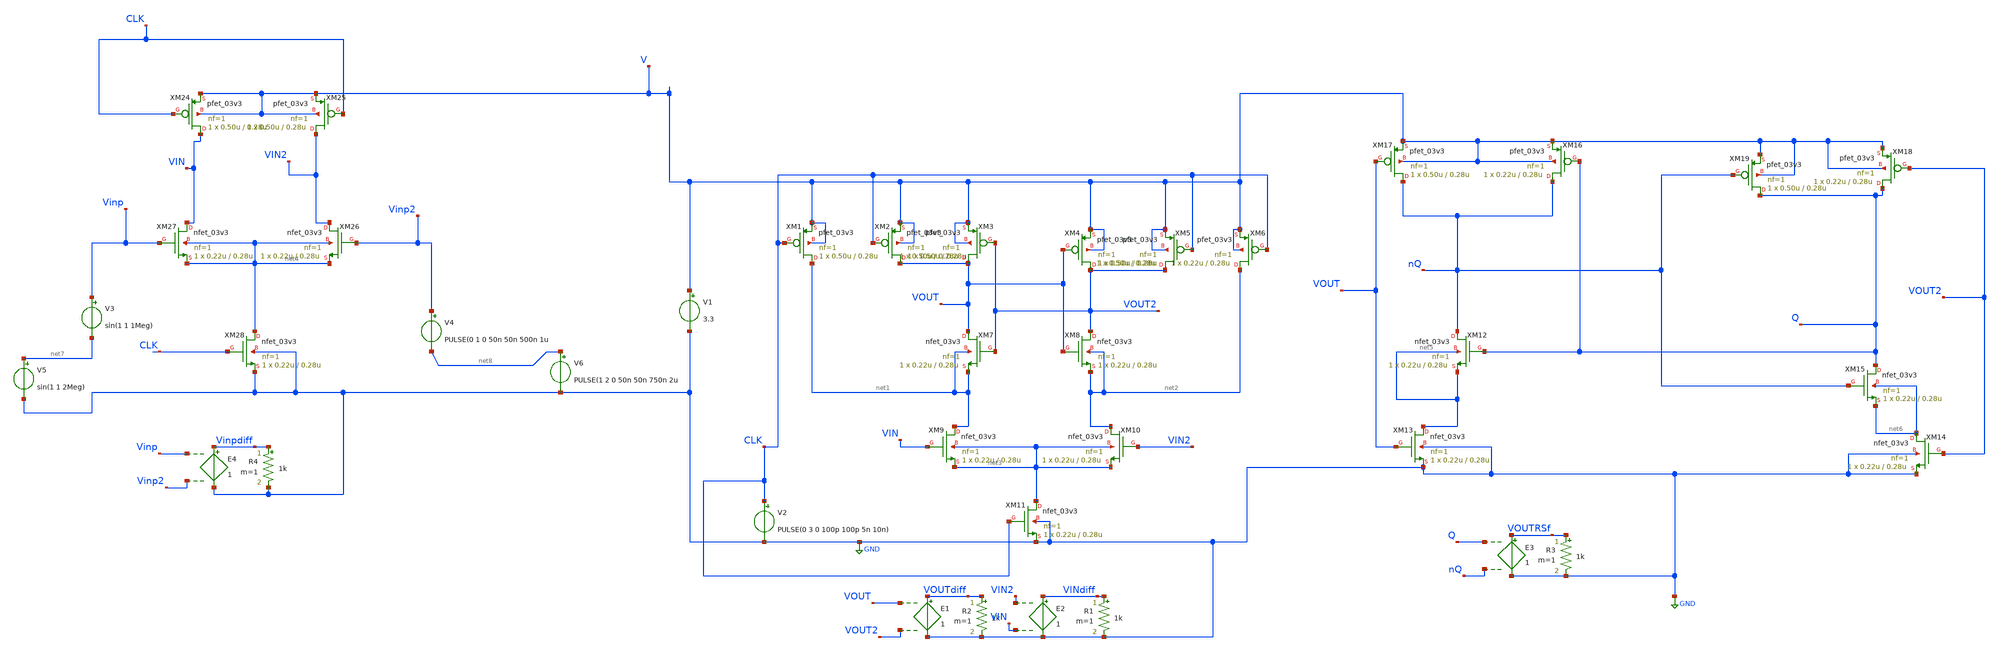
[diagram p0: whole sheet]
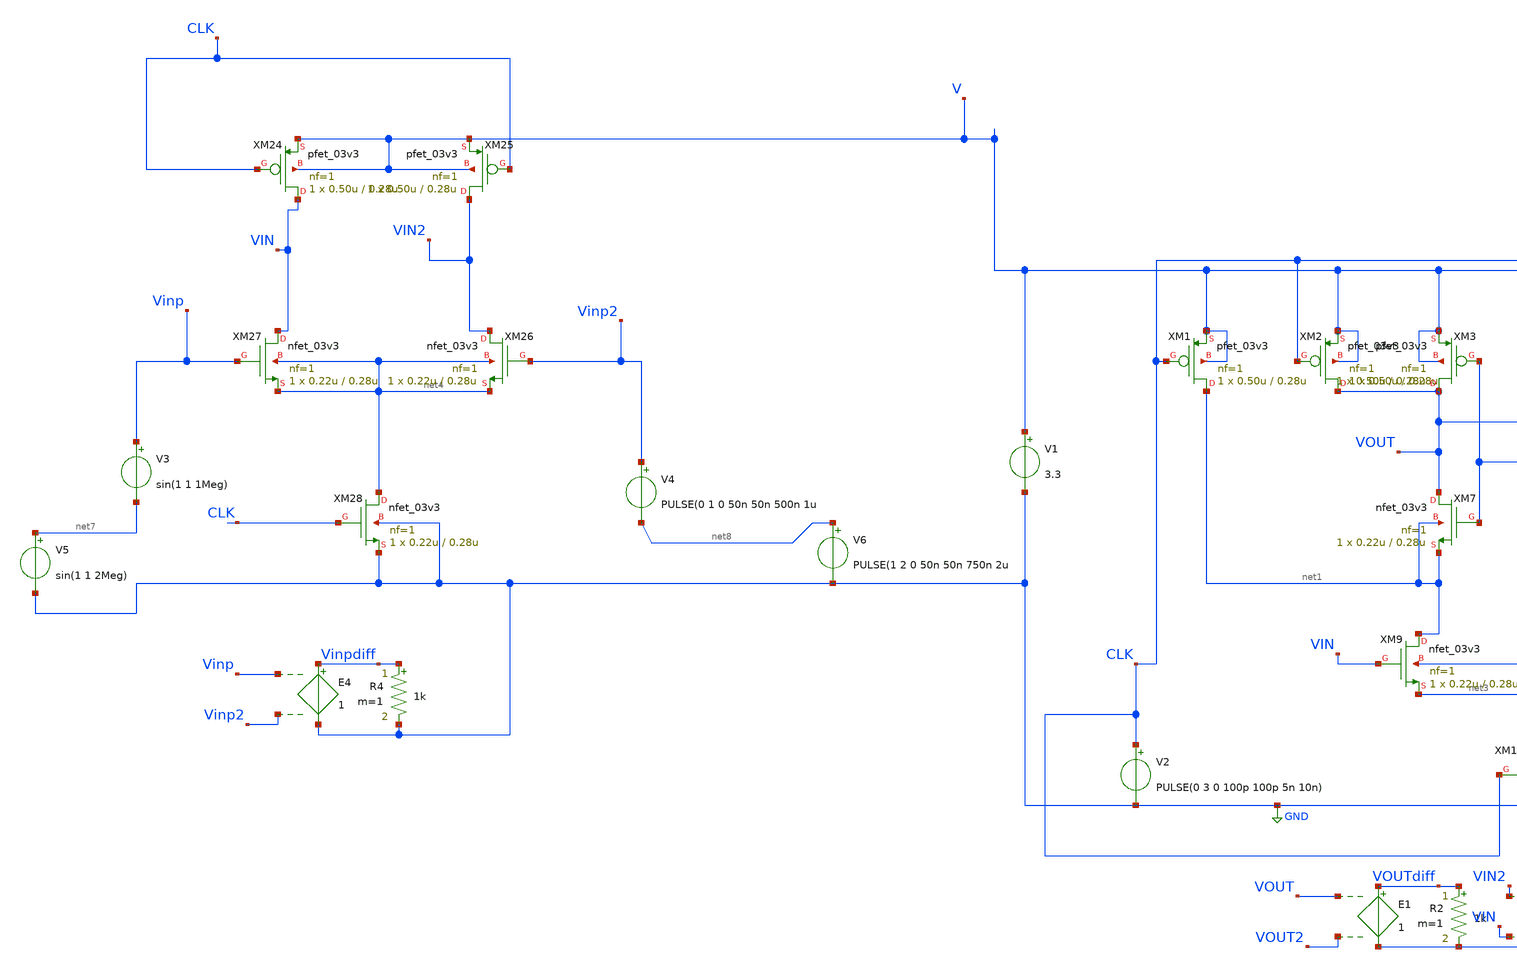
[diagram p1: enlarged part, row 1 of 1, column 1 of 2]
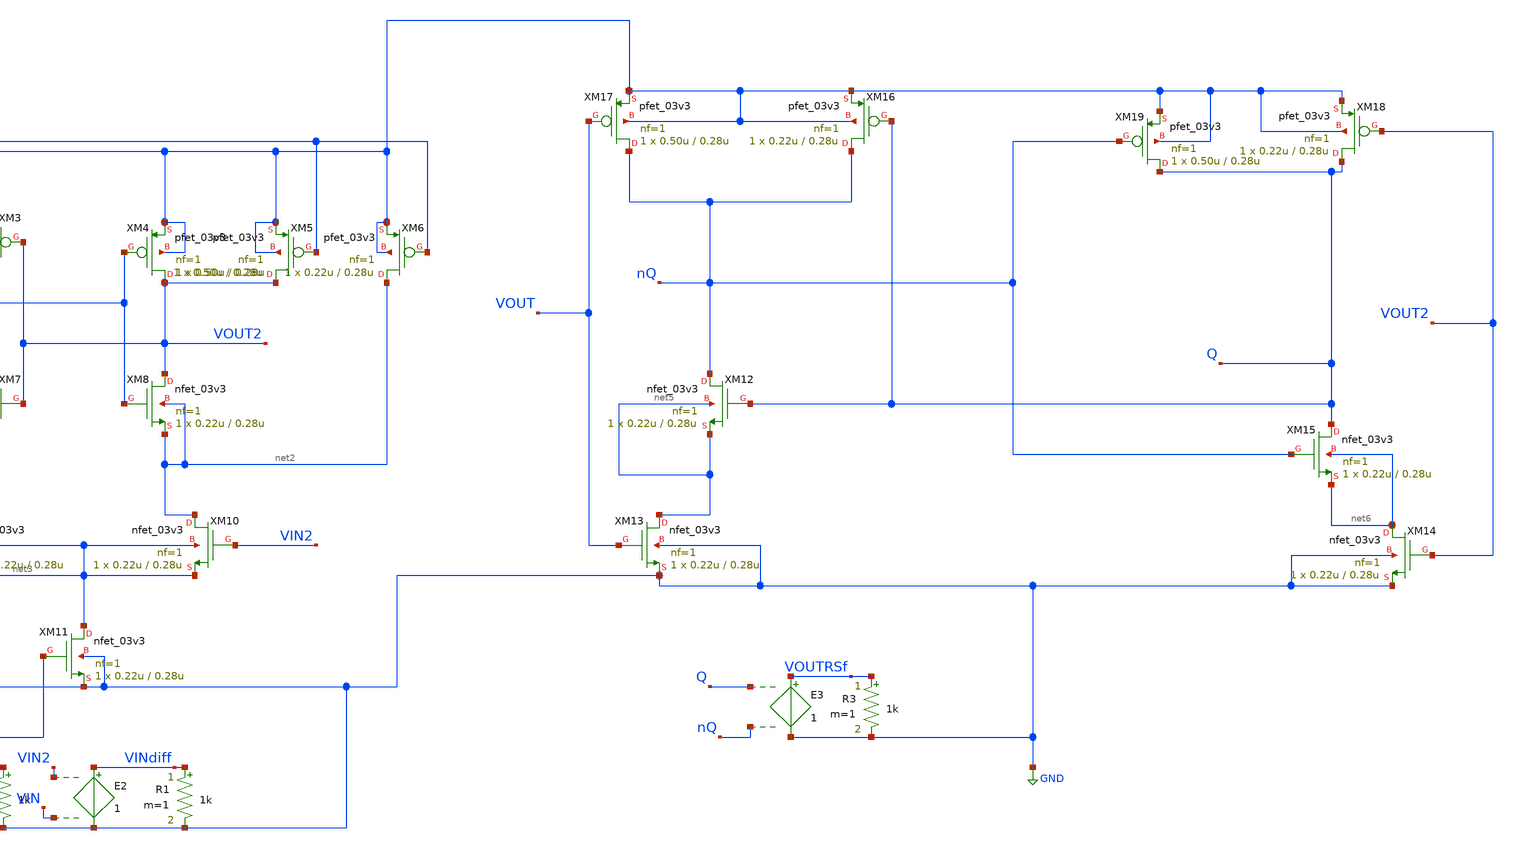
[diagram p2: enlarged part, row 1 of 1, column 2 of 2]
** sch_path: old/StrongArm2.sch
**.subckt StrongArm2
XM1 net1 CLK V V pfet_03v3 L=0.28u W=0.50u nf=1 ad='int((nf+1)/2) * W/nf * 0.18u' as='int((nf+2)/2) * W/nf * 0.18u'
+ pd='2*int((nf+1)/2) * (W/nf + 0.18u)' ps='2*int((nf+2)/2) * (W/nf + 0.18u)' nrd='0.18u / W' nrs='0.18u / W'
+ sa=0 sb=0 sd=0 m=1
XM2 VOUT CLK V V pfet_03v3 L=0.28u W=0.50u nf=1 ad='int((nf+1)/2) * W/nf * 0.18u' as='int((nf+2)/2) * W/nf * 0.18u'
+ pd='2*int((nf+1)/2) * (W/nf + 0.18u)' ps='2*int((nf+2)/2) * (W/nf + 0.18u)' nrd='0.18u / W' nrs='0.18u / W'
+ sa=0 sb=0 sd=0 m=1
XM3 VOUT VOUT2 V V pfet_03v3 L=0.28u W=0.50u nf=1 ad='int((nf+1)/2) * W/nf * 0.18u' as='int((nf+2)/2) * W/nf * 0.18u'
+ pd='2*int((nf+1)/2) * (W/nf + 0.18u)' ps='2*int((nf+2)/2) * (W/nf + 0.18u)' nrd='0.18u / W' nrs='0.18u / W'
+ sa=0 sb=0 sd=0 m=1
XM4 VOUT2 VOUT V V pfet_03v3 L=0.28u W=0.50u nf=1 ad='int((nf+1)/2) * W/nf * 0.18u' as='int((nf+2)/2) * W/nf * 0.18u'
+ pd='2*int((nf+1)/2) * (W/nf + 0.18u)' ps='2*int((nf+2)/2) * (W/nf + 0.18u)' nrd='0.18u / W' nrs='0.18u / W'
+ sa=0 sb=0 sd=0 m=1
XM5 VOUT2 CLK V V pfet_03v3 L=0.28u W=0.50u nf=1 ad='int((nf+1)/2) * W/nf * 0.18u' as='int((nf+2)/2) * W/nf * 0.18u'
+ pd='2*int((nf+1)/2) * (W/nf + 0.18u)' ps='2*int((nf+2)/2) * (W/nf + 0.18u)' nrd='0.18u / W' nrs='0.18u / W'
+ sa=0 sb=0 sd=0 m=1
XM6 net2 CLK V V pfet_03v3 L=0.28u W=0.22u nf=1 ad='int((nf+1)/2) * W/nf * 0.18u' as='int((nf+2)/2) * W/nf * 0.18u'
+ pd='2*int((nf+1)/2) * (W/nf + 0.18u)' ps='2*int((nf+2)/2) * (W/nf + 0.18u)' nrd='0.18u / W' nrs='0.18u / W'
+ sa=0 sb=0 sd=0 m=1
XM7 VOUT VOUT2 net1 net1 nfet_03v3 L=0.28u W=0.22u nf=1 ad='int((nf+1)/2) * W/nf * 0.18u' as='int((nf+2)/2) * W/nf * 0.18u'
+ pd='2*int((nf+1)/2) * (W/nf + 0.18u)' ps='2*int((nf+2)/2) * (W/nf + 0.18u)' nrd='0.18u / W' nrs='0.18u / W'
+ sa=0 sb=0 sd=0 m=1
XM8 VOUT2 VOUT net2 net2 nfet_03v3 L=0.28u W=0.22u nf=1 ad='int((nf+1)/2) * W/nf * 0.18u' as='int((nf+2)/2) * W/nf * 0.18u'
+ pd='2*int((nf+1)/2) * (W/nf + 0.18u)' ps='2*int((nf+2)/2) * (W/nf + 0.18u)' nrd='0.18u / W' nrs='0.18u / W'
+ sa=0 sb=0 sd=0 m=1
XM9 net1 VIN net3 net3 nfet_03v3 L=0.28u W=0.22u nf=1 ad='int((nf+1)/2) * W/nf * 0.18u' as='int((nf+2)/2) * W/nf * 0.18u'
+ pd='2*int((nf+1)/2) * (W/nf + 0.18u)' ps='2*int((nf+2)/2) * (W/nf + 0.18u)' nrd='0.18u / W' nrs='0.18u / W'
+ sa=0 sb=0 sd=0 m=1
XM10 net2 VIN2 net3 net3 nfet_03v3 L=0.28u W=0.22u nf=1 ad='int((nf+1)/2) * W/nf * 0.18u' as='int((nf+2)/2) * W/nf * 0.18u'
+ pd='2*int((nf+1)/2) * (W/nf + 0.18u)' ps='2*int((nf+2)/2) * (W/nf + 0.18u)' nrd='0.18u / W' nrs='0.18u / W'
+ sa=0 sb=0 sd=0 m=1
XM11 net3 CLK GND GND nfet_03v3 L=0.28u W=0.22u nf=1 ad='int((nf+1)/2) * W/nf * 0.18u' as='int((nf+2)/2) * W/nf * 0.18u'
+ pd='2*int((nf+1)/2) * (W/nf + 0.18u)' ps='2*int((nf+2)/2) * (W/nf + 0.18u)' nrd='0.18u / W' nrs='0.18u / W'
+ sa=0 sb=0 sd=0 m=1
V1 V GND 3.3
V2 CLK GND PULSE(0 3 0 100p 100p 5n 10n)
R2 VOUTdiff GND 1k m=1
E1 VOUTdiff GND VOUT VOUT2 1
R1 VINdiff GND 1k m=1
E2 VINdiff GND VIN2 VIN 1
XM12 nQ Q net5 net5 nfet_03v3 L=0.28u W=0.22u nf=1 ad='int((nf+1)/2) * W/nf * 0.18u' as='int((nf+2)/2) * W/nf * 0.18u'
+ pd='2*int((nf+1)/2) * (W/nf + 0.18u)' ps='2*int((nf+2)/2) * (W/nf + 0.18u)' nrd='0.18u / W' nrs='0.18u / W'
+ sa=0 sb=0 sd=0 m=1
XM13 net5 VOUT GND GND nfet_03v3 L=0.28u W=0.22u nf=1 ad='int((nf+1)/2) * W/nf * 0.18u' as='int((nf+2)/2) * W/nf * 0.18u'
+ pd='2*int((nf+1)/2) * (W/nf + 0.18u)' ps='2*int((nf+2)/2) * (W/nf + 0.18u)' nrd='0.18u / W' nrs='0.18u / W'
+ sa=0 sb=0 sd=0 m=1
XM14 net6 VOUT2 GND GND nfet_03v3 L=0.28u W=0.22u nf=1 ad='int((nf+1)/2) * W/nf * 0.18u' as='int((nf+2)/2) * W/nf * 0.18u'
+ pd='2*int((nf+1)/2) * (W/nf + 0.18u)' ps='2*int((nf+2)/2) * (W/nf + 0.18u)' nrd='0.18u / W' nrs='0.18u / W'
+ sa=0 sb=0 sd=0 m=1
XM15 Q nQ net6 net6 nfet_03v3 L=0.28u W=0.22u nf=1 ad='int((nf+1)/2) * W/nf * 0.18u' as='int((nf+2)/2) * W/nf * 0.18u'
+ pd='2*int((nf+1)/2) * (W/nf + 0.18u)' ps='2*int((nf+2)/2) * (W/nf + 0.18u)' nrd='0.18u / W' nrs='0.18u / W'
+ sa=0 sb=0 sd=0 m=1
XM16 nQ Q V V pfet_03v3 L=0.28u W=0.22u nf=1 ad='int((nf+1)/2) * W/nf * 0.18u' as='int((nf+2)/2) * W/nf * 0.18u'
+ pd='2*int((nf+1)/2) * (W/nf + 0.18u)' ps='2*int((nf+2)/2) * (W/nf + 0.18u)' nrd='0.18u / W' nrs='0.18u / W'
+ sa=0 sb=0 sd=0 m=1
XM17 nQ VOUT V V pfet_03v3 L=0.28u W=0.50u nf=1 ad='int((nf+1)/2) * W/nf * 0.18u' as='int((nf+2)/2) * W/nf * 0.18u'
+ pd='2*int((nf+1)/2) * (W/nf + 0.18u)' ps='2*int((nf+2)/2) * (W/nf + 0.18u)' nrd='0.18u / W' nrs='0.18u / W'
+ sa=0 sb=0 sd=0 m=1
XM18 Q VOUT2 V V pfet_03v3 L=0.28u W=0.22u nf=1 ad='int((nf+1)/2) * W/nf * 0.18u' as='int((nf+2)/2) * W/nf * 0.18u'
+ pd='2*int((nf+1)/2) * (W/nf + 0.18u)' ps='2*int((nf+2)/2) * (W/nf + 0.18u)' nrd='0.18u / W' nrs='0.18u / W'
+ sa=0 sb=0 sd=0 m=1
XM19 Q nQ V V pfet_03v3 L=0.28u W=0.50u nf=1 ad='int((nf+1)/2) * W/nf * 0.18u' as='int((nf+2)/2) * W/nf * 0.18u'
+ pd='2*int((nf+1)/2) * (W/nf + 0.18u)' ps='2*int((nf+2)/2) * (W/nf + 0.18u)' nrd='0.18u / W' nrs='0.18u / W'
+ sa=0 sb=0 sd=0 m=1
R3 VOUTRSf GND 1k m=1
E3 VOUTRSf GND Q nQ 1
XM26 VIN2 Vinp2 net4 net4 nfet_03v3 L=0.28u W=0.22u nf=1 ad='int((nf+1)/2) * W/nf * 0.18u' as='int((nf+2)/2) * W/nf * 0.18u'
+ pd='2*int((nf+1)/2) * (W/nf + 0.18u)' ps='2*int((nf+2)/2) * (W/nf + 0.18u)' nrd='0.18u / W' nrs='0.18u / W'
+ sa=0 sb=0 sd=0 m=1
XM27 VIN Vinp net4 net4 nfet_03v3 L=0.28u W=0.22u nf=1 ad='int((nf+1)/2) * W/nf * 0.18u' as='int((nf+2)/2) * W/nf * 0.18u'
+ pd='2*int((nf+1)/2) * (W/nf + 0.18u)' ps='2*int((nf+2)/2) * (W/nf + 0.18u)' nrd='0.18u / W' nrs='0.18u / W'
+ sa=0 sb=0 sd=0 m=1
V3 Vinp net7 sin(1 1 1Meg)
V4 Vinp2 net8 PULSE(0 1 0 50n 50n 500n 1u
R4 Vinpdiff GND 1k m=1
E4 Vinpdiff GND Vinp Vinp2 1
XM28 net4 CLK GND GND nfet_03v3 L=0.28u W=0.22u nf=1 ad='int((nf+1)/2) * W/nf * 0.18u' as='int((nf+2)/2) * W/nf * 0.18u'
+ pd='2*int((nf+1)/2) * (W/nf + 0.18u)' ps='2*int((nf+2)/2) * (W/nf + 0.18u)' nrd='0.18u / W' nrs='0.18u / W'
+ sa=0 sb=0 sd=0 m=1
XM24 VIN CLK V V pfet_03v3 L=0.28u W=0.50u nf=1 ad='int((nf+1)/2) * W/nf * 0.18u' as='int((nf+2)/2) * W/nf * 0.18u'
+ pd='2*int((nf+1)/2) * (W/nf + 0.18u)' ps='2*int((nf+2)/2) * (W/nf + 0.18u)' nrd='0.18u / W' nrs='0.18u / W'
+ sa=0 sb=0 sd=0 m=1
XM25 VIN2 CLK V V pfet_03v3 L=0.28u W=0.50u nf=1 ad='int((nf+1)/2) * W/nf * 0.18u' as='int((nf+2)/2) * W/nf * 0.18u'
+ pd='2*int((nf+1)/2) * (W/nf + 0.18u)' ps='2*int((nf+2)/2) * (W/nf + 0.18u)' nrd='0.18u / W' nrs='0.18u / W'
+ sa=0 sb=0 sd=0 m=1
V5 net7 GND sin(1 1 2Meg)
V6 net8 GND PULSE(1 2 0 50n 50n 750n 2u
**** begin user architecture code


.control
save all
tran 100p 10u 30n
plot VOUTrsf Vinpdiff
plot VOUTdiff Vinpdiff
plot  Vinpdiff Vindiff
plot VOUTdiff VOUTrsf
plot VOUT VOUT2
.endc


.include /foss/pdks/gf180mcuC/libs.tech/ngspice/design.ngspice
.lib /foss/pdks/gf180mcuC/libs.tech/ngspice/sm141064.ngspice typical

**** end user architecture code
**.ends
.GLOBAL GND
.end
